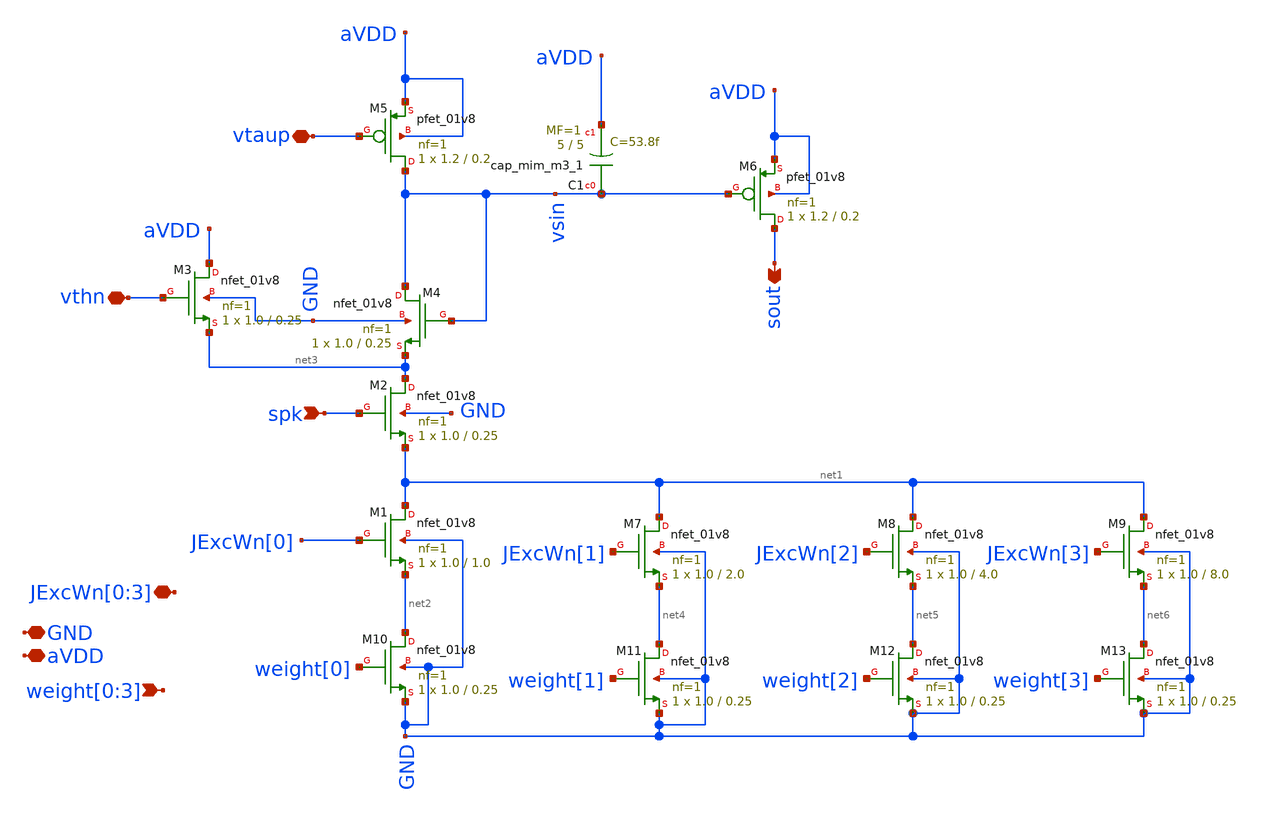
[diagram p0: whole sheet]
** sch_path: design/xschem/dpi_syn_exc_4bit_fc_v2_norail.sch
**.subckt dpi_syn_exc_4bit_fc_v2_norail GND aVDD vtaup spk sout vthn
*+ weight[0],weight[1],weight[2],weight[3] JExcWn[0],JExcWn[1],JExcWn[2],JExcWn[3]
*.iopin GND
*.iopin aVDD
*.iopin vtaup
*.ipin spk
*.opin sout
*.iopin vthn
*.ipin weight[0],weight[1],weight[2],weight[3]
*.iopin JExcWn[0],JExcWn[1],JExcWn[2],JExcWn[3]
XM2 net3 spk net1 GND sky130_fd_pr__nfet_01v8 L=0.25 W=1.0 nf=1 ad='int((nf+1)/2) * W/nf * 0.29' as='int((nf+2)/2) * W/nf * 0.29'
+ pd='2*int((nf+1)/2) * (W/nf + 0.29)' ps='2*int((nf+2)/2) * (W/nf + 0.29)' nrd='0.29 / W' nrs='0.29 / W'
+ sa=0 sb=0 sd=0 mult=1 m=1
XC1 vsin aVDD sky130_fd_pr__cap_mim_m3_1 W=5 L=5 MF=1 m=1
XM5 vsin vtaup aVDD aVDD sky130_fd_pr__pfet_01v8 L=0.2 W=1.2 nf=1 ad='int((nf+1)/2) * W/nf * 0.29' as='int((nf+2)/2) * W/nf * 0.29'
+ pd='2*int((nf+1)/2) * (W/nf + 0.29)' ps='2*int((nf+2)/2) * (W/nf + 0.29)' nrd='0.29 / W' nrs='0.29 / W'
+ sa=0 sb=0 sd=0 mult=1 m=1
XM6 sout vsin aVDD aVDD sky130_fd_pr__pfet_01v8 L=0.2 W=1.2 nf=1 ad='int((nf+1)/2) * W/nf * 0.29' as='int((nf+2)/2) * W/nf * 0.29'
+ pd='2*int((nf+1)/2) * (W/nf + 0.29)' ps='2*int((nf+2)/2) * (W/nf + 0.29)' nrd='0.29 / W' nrs='0.29 / W'
+ sa=0 sb=0 sd=0 mult=1 m=1
XM1 net1 JExcWn[0] net2 GND sky130_fd_pr__nfet_01v8 L=1.0 W=1.0 nf=1 ad='int((nf+1)/2) * W/nf * 0.29'
+ as='int((nf+2)/2) * W/nf * 0.29' pd='2*int((nf+1)/2) * (W/nf + 0.29)' ps='2*int((nf+2)/2) * (W/nf + 0.29)'
+ nrd='0.29 / W' nrs='0.29 / W' sa=0 sb=0 sd=0 mult=1 m=1
XM4 vsin vsin net3 GND sky130_fd_pr__nfet_01v8 L=0.25 W=1.0 nf=1 ad='int((nf+1)/2) * W/nf * 0.29' as='int((nf+2)/2) * W/nf * 0.29'
+ pd='2*int((nf+1)/2) * (W/nf + 0.29)' ps='2*int((nf+2)/2) * (W/nf + 0.29)' nrd='0.29 / W' nrs='0.29 / W'
+ sa=0 sb=0 sd=0 mult=1 m=1
XM3 aVDD vthn net3 GND sky130_fd_pr__nfet_01v8 L=0.25 W=1.0 nf=1 ad='int((nf+1)/2) * W/nf * 0.29' as='int((nf+2)/2) * W/nf * 0.29'
+ pd='2*int((nf+1)/2) * (W/nf + 0.29)' ps='2*int((nf+2)/2) * (W/nf + 0.29)' nrd='0.29 / W' nrs='0.29 / W'
+ sa=0 sb=0 sd=0 mult=1 m=1
XM7 net1 JExcWn[1] net4 GND sky130_fd_pr__nfet_01v8 L=2.0 W=1.0 nf=1 ad='int((nf+1)/2) * W/nf * 0.29'
+ as='int((nf+2)/2) * W/nf * 0.29' pd='2*int((nf+1)/2) * (W/nf + 0.29)' ps='2*int((nf+2)/2) * (W/nf + 0.29)'
+ nrd='0.29 / W' nrs='0.29 / W' sa=0 sb=0 sd=0 mult=1 m=1
XM8 net1 JExcWn[2] net5 GND sky130_fd_pr__nfet_01v8 L=4.0 W=1.0 nf=1 ad='int((nf+1)/2) * W/nf * 0.29'
+ as='int((nf+2)/2) * W/nf * 0.29' pd='2*int((nf+1)/2) * (W/nf + 0.29)' ps='2*int((nf+2)/2) * (W/nf + 0.29)'
+ nrd='0.29 / W' nrs='0.29 / W' sa=0 sb=0 sd=0 mult=1 m=1
XM9 net1 JExcWn[3] net6 GND sky130_fd_pr__nfet_01v8 L=8.0 W=1.0 nf=1 ad='int((nf+1)/2) * W/nf * 0.29'
+ as='int((nf+2)/2) * W/nf * 0.29' pd='2*int((nf+1)/2) * (W/nf + 0.29)' ps='2*int((nf+2)/2) * (W/nf + 0.29)'
+ nrd='0.29 / W' nrs='0.29 / W' sa=0 sb=0 sd=0 mult=1 m=1
XM10 net2 weight[0] GND GND sky130_fd_pr__nfet_01v8 L=0.25 W=1.0 nf=1 ad='int((nf+1)/2) * W/nf * 0.29'
+ as='int((nf+2)/2) * W/nf * 0.29' pd='2*int((nf+1)/2) * (W/nf + 0.29)' ps='2*int((nf+2)/2) * (W/nf + 0.29)'
+ nrd='0.29 / W' nrs='0.29 / W' sa=0 sb=0 sd=0 mult=1 m=1
XM11 net4 weight[1] GND GND sky130_fd_pr__nfet_01v8 L=0.25 W=1.0 nf=1 ad='int((nf+1)/2) * W/nf * 0.29'
+ as='int((nf+2)/2) * W/nf * 0.29' pd='2*int((nf+1)/2) * (W/nf + 0.29)' ps='2*int((nf+2)/2) * (W/nf + 0.29)'
+ nrd='0.29 / W' nrs='0.29 / W' sa=0 sb=0 sd=0 mult=1 m=1
XM12 net5 weight[2] GND GND sky130_fd_pr__nfet_01v8 L=0.25 W=1.0 nf=1 ad='int((nf+1)/2) * W/nf * 0.29'
+ as='int((nf+2)/2) * W/nf * 0.29' pd='2*int((nf+1)/2) * (W/nf + 0.29)' ps='2*int((nf+2)/2) * (W/nf + 0.29)'
+ nrd='0.29 / W' nrs='0.29 / W' sa=0 sb=0 sd=0 mult=1 m=1
XM13 net6 weight[3] GND GND sky130_fd_pr__nfet_01v8 L=0.25 W=1.0 nf=1 ad='int((nf+1)/2) * W/nf * 0.29'
+ as='int((nf+2)/2) * W/nf * 0.29' pd='2*int((nf+1)/2) * (W/nf + 0.29)' ps='2*int((nf+2)/2) * (W/nf + 0.29)'
+ nrd='0.29 / W' nrs='0.29 / W' sa=0 sb=0 sd=0 mult=1 m=1
**.ends
.end
